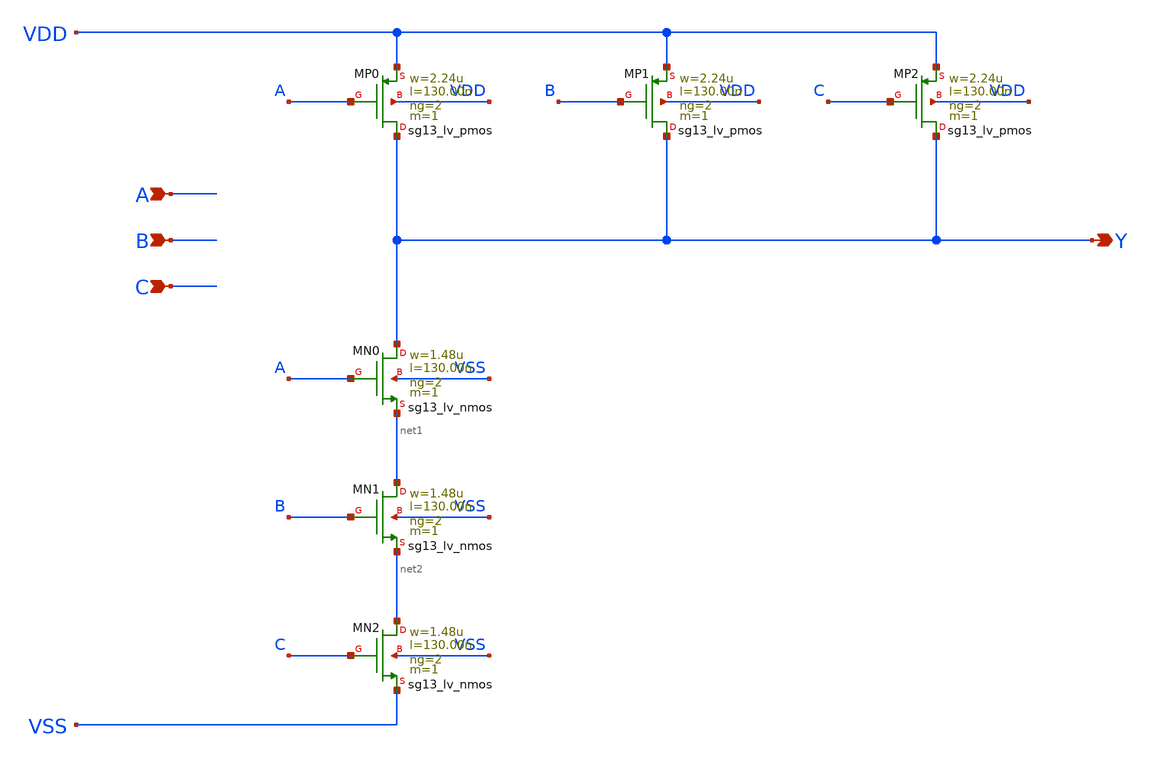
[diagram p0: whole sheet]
** sch_path: outputs/sg13g2_cells/cells/sg13g2_nand3_2/sg13g2_nand3_2.sch
**.subckt sg13g2_nand3_2 A B C Y
*.ipin A
*.ipin B
*.ipin C
*.opin Y
XMN1 net1 B net2 VSS sg13_lv_nmos w=1.48u l=130.00n ng=2 m=1 mm_ok=1
XMN2 net2 C VSS VSS sg13_lv_nmos w=1.48u l=130.00n ng=2 m=1 mm_ok=1
XMN0 Y A net1 VSS sg13_lv_nmos w=1.48u l=130.00n ng=2 m=1 mm_ok=1
XMP0 Y A VDD VDD sg13_lv_pmos w=2.24u l=130.00n ng=2 m=1 mm_ok=1
XMP1 Y B VDD VDD sg13_lv_pmos w=2.24u l=130.00n ng=2 m=1 mm_ok=1
XMP2 Y C VDD VDD sg13_lv_pmos w=2.24u l=130.00n ng=2 m=1 mm_ok=1
**.ends
.end
